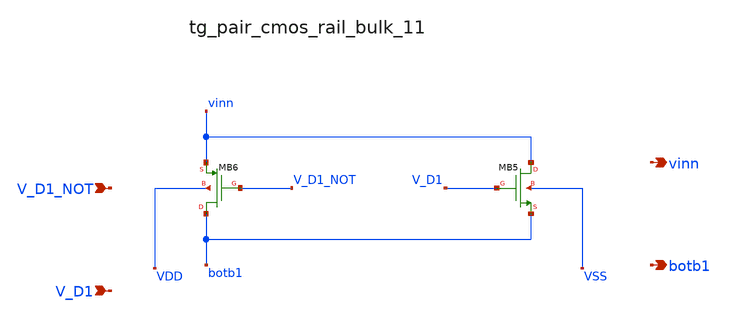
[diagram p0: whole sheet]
** sch_path: analog-db/raw/ia_005_hsu_pga_ideal/hier/blocks/tg_pair_cmos_rail_bulk_11.sch
**.subckt tg_pair_cmos_rail_bulk_11 V_D1_NOT V_D1 vinn botb1
*.ipin V_D1_NOT
*.ipin V_D1
*.opin vinn
*.opin botb1
XMB5 vinn V_D1 botb1 VSS sg13_lv_nmos w=x_dut_xmb5_w l=x_dut_xmb5_l ng=1 m=x_dut_xmb5_m
XMB6 botb1 V_D1_NOT vinn VDD sg13_lv_pmos w=x_dut_xmb6_w l=x_dut_xmb6_l ng=1 m=x_dut_xmb6_m
**.ends
.end
